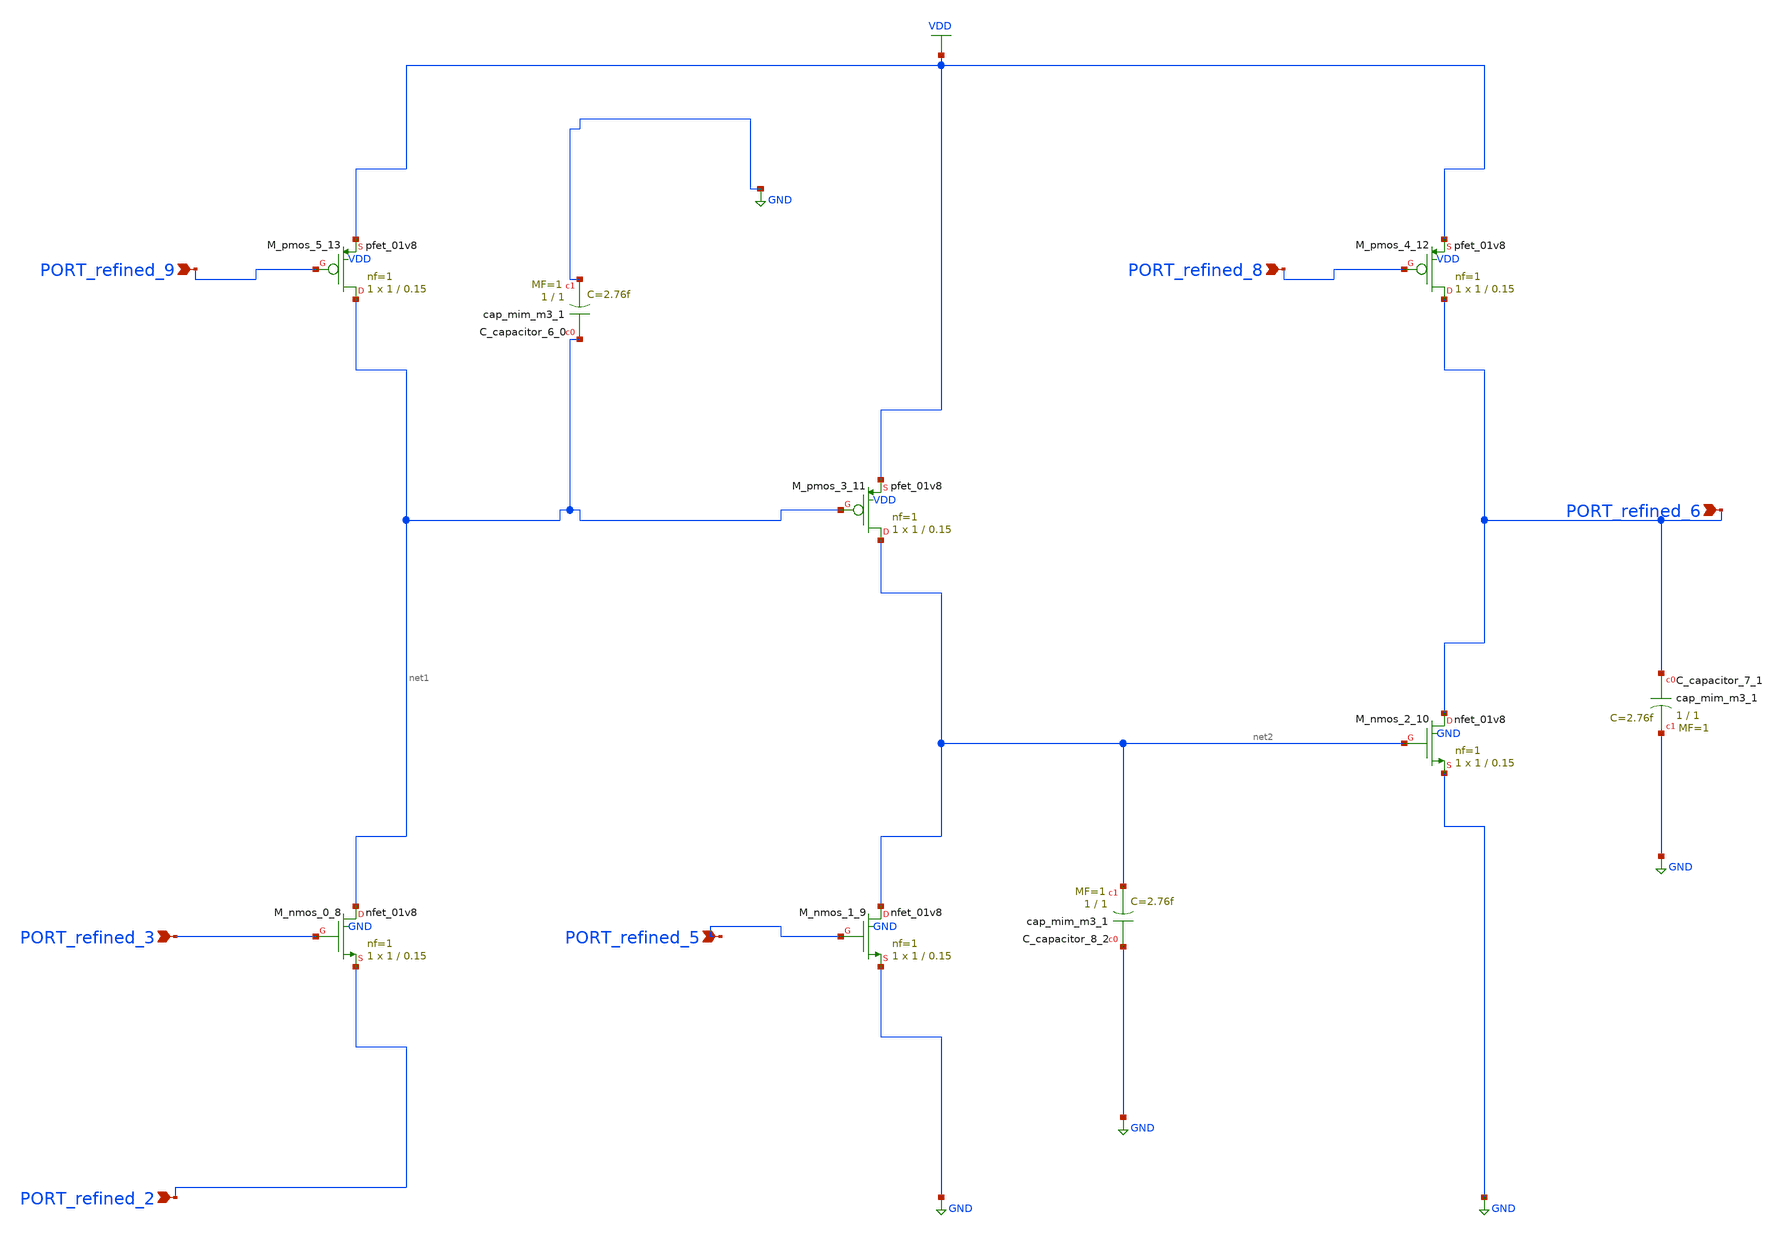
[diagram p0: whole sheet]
** sch_path: schematics/10_1007_s00034-017-0630-6_05_001_crop2.sch
**.subckt 10_1007_s00034-017-0630-6_05_001_crop2 PORT_refined_6 PORT_refined_8 PORT_refined_3
*+ PORT_refined_9 PORT_refined_2 PORT_refined_5
*.ipin PORT_refined_6
*.ipin PORT_refined_8
*.ipin PORT_refined_3
*.ipin PORT_refined_9
*.ipin PORT_refined_2
*.ipin PORT_refined_5
XC_capacitor_6_0 net1 GND sky130_fd_pr__cap_mim_m3_1 W=1 L=1 MF=1 m=1
XC_capacitor_7_1 PORT_refined_6 GND sky130_fd_pr__cap_mim_m3_1 W=1 L=1 MF=1 m=1
XC_capacitor_8_2 GND net2 sky130_fd_pr__cap_mim_m3_1 W=1 L=1 MF=1 m=1
XM_nmos_0_8 net1 PORT_refined_3 PORT_refined_2 GND sky130_fd_pr__nfet_01v8 L=0.15 W=1 nf=1 ad='int((1 + 1)/2) * 1 / 1 * 0.29'
+ as='int((1 + 2)/2) * 1 / 1 * 0.29' pd='2*int((1 + 1)/2) * (1 / 1 + 0.29)' ps='2*int((1 + 2)/2) * (1 / 1 + 0.29)'
+ nrd='0.29 / 1 ' nrs='0.29 / 1 ' sa=0 sb=0 sd=0 mult=1 m=1
XM_nmos_1_9 net2 PORT_refined_5 GND GND sky130_fd_pr__nfet_01v8 L=0.15 W=1 nf=1 ad='int((1 + 1)/2) * 1 / 1 * 0.29'
+ as='int((1 + 2)/2) * 1 / 1 * 0.29' pd='2*int((1 + 1)/2) * (1 / 1 + 0.29)' ps='2*int((1 + 2)/2) * (1 / 1 + 0.29)'
+ nrd='0.29 / 1 ' nrs='0.29 / 1 ' sa=0 sb=0 sd=0 mult=1 m=1
XM_nmos_2_10 PORT_refined_6 net2 GND GND sky130_fd_pr__nfet_01v8 L=0.15 W=1 nf=1 ad='int((1 + 1)/2) * 1 / 1 * 0.29'
+ as='int((1 + 2)/2) * 1 / 1 * 0.29' pd='2*int((1 + 1)/2) * (1 / 1 + 0.29)' ps='2*int((1 + 2)/2) * (1 / 1 + 0.29)'
+ nrd='0.29 / 1 ' nrs='0.29 / 1 ' sa=0 sb=0 sd=0 mult=1 m=1
XM_pmos_3_11 net2 net1 VDD VDD sky130_fd_pr__pfet_01v8 L=0.15 W=1 nf=1 ad='int((1 + 1)/2) * 1 / 1 * 0.29'
+ as='int((1 + 2)/2) * 1 / 1 * 0.29' pd='2*int((1 + 1)/2) * (1 / 1 + 0.29)' ps='2*int((1 + 2)/2) * (1 / 1 + 0.29)'
+ nrd='0.29 / 1 ' nrs='0.29 / 1 ' sa=0 sb=0 sd=0 mult=1 m=1
XM_pmos_4_12 PORT_refined_6 PORT_refined_8 VDD VDD sky130_fd_pr__pfet_01v8 L=0.15 W=1 nf=1 ad='int((1 + 1)/2) * 1 / 1 * 0.29'
+ as='int((1 + 2)/2) * 1 / 1 * 0.29' pd='2*int((1 + 1)/2) * (1 / 1 + 0.29)' ps='2*int((1 + 2)/2) * (1 / 1 + 0.29)'
+ nrd='0.29 / 1 ' nrs='0.29 / 1 ' sa=0 sb=0 sd=0 mult=1 m=1
XM_pmos_5_13 net1 PORT_refined_9 VDD VDD sky130_fd_pr__pfet_01v8 L=0.15 W=1 nf=1 ad='int((1 + 1)/2) * 1 / 1 * 0.29'
+ as='int((1 + 2)/2) * 1 / 1 * 0.29' pd='2*int((1 + 1)/2) * (1 / 1 + 0.29)' ps='2*int((1 + 2)/2) * (1 / 1 + 0.29)'
+ nrd='0.29 / 1 ' nrs='0.29 / 1 ' sa=0 sb=0 sd=0 mult=1 m=1
**.ends
.GLOBAL GND
.GLOBAL VDD
.end
